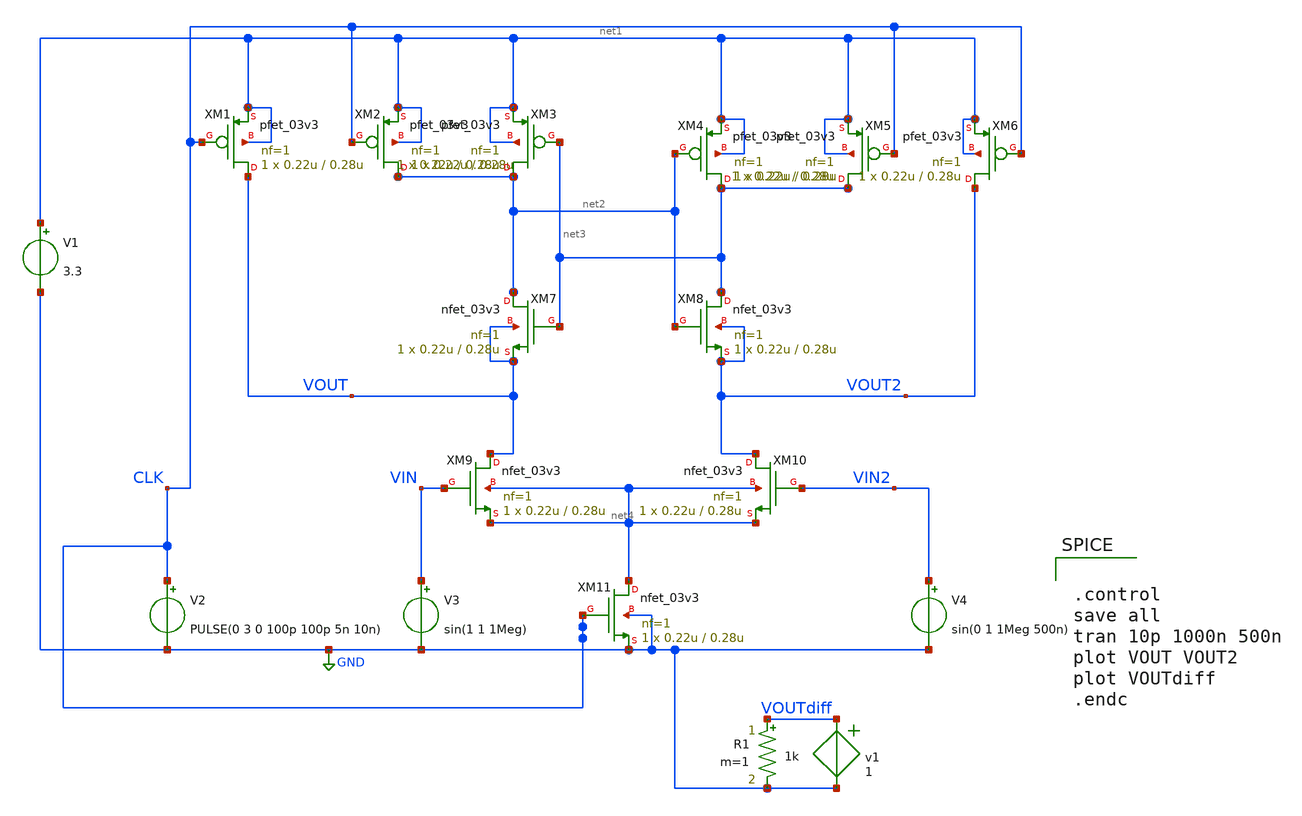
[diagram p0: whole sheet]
** sch_path: StrongARM.sch
**.subckt StrongARM
XM1 VOUT CLK net1 net1 pfet_03v3 L=0.28u W=0.22u nf=1 ad='int((nf+1)/2) * W/nf * 0.18u' as='int((nf+2)/2) * W/nf * 0.18u'
+ pd='2*int((nf+1)/2) * (W/nf + 0.18u)' ps='2*int((nf+2)/2) * (W/nf + 0.18u)' nrd='0.18u / W' nrs='0.18u / W'
+ sa=0 sb=0 sd=0 m=1
XM2 net2 CLK net1 net1 pfet_03v3 L=0.28u W=0.22u nf=1 ad='int((nf+1)/2) * W/nf * 0.18u' as='int((nf+2)/2) * W/nf * 0.18u'
+ pd='2*int((nf+1)/2) * (W/nf + 0.18u)' ps='2*int((nf+2)/2) * (W/nf + 0.18u)' nrd='0.18u / W' nrs='0.18u / W'
+ sa=0 sb=0 sd=0 m=1
XM3 net2 net3 net1 net1 pfet_03v3 L=0.28u W=0.22u nf=1 ad='int((nf+1)/2) * W/nf * 0.18u' as='int((nf+2)/2) * W/nf * 0.18u'
+ pd='2*int((nf+1)/2) * (W/nf + 0.18u)' ps='2*int((nf+2)/2) * (W/nf + 0.18u)' nrd='0.18u / W' nrs='0.18u / W'
+ sa=0 sb=0 sd=0 m=1
XM4 net3 net2 net1 net1 pfet_03v3 L=0.28u W=0.22u nf=1 ad='int((nf+1)/2) * W/nf * 0.18u' as='int((nf+2)/2) * W/nf * 0.18u'
+ pd='2*int((nf+1)/2) * (W/nf + 0.18u)' ps='2*int((nf+2)/2) * (W/nf + 0.18u)' nrd='0.18u / W' nrs='0.18u / W'
+ sa=0 sb=0 sd=0 m=1
XM5 net3 CLK net1 net1 pfet_03v3 L=0.28u W=0.22u nf=1 ad='int((nf+1)/2) * W/nf * 0.18u' as='int((nf+2)/2) * W/nf * 0.18u'
+ pd='2*int((nf+1)/2) * (W/nf + 0.18u)' ps='2*int((nf+2)/2) * (W/nf + 0.18u)' nrd='0.18u / W' nrs='0.18u / W'
+ sa=0 sb=0 sd=0 m=1
XM6 VOUT2 CLK net1 net1 pfet_03v3 L=0.28u W=0.22u nf=1 ad='int((nf+1)/2) * W/nf * 0.18u' as='int((nf+2)/2) * W/nf * 0.18u'
+ pd='2*int((nf+1)/2) * (W/nf + 0.18u)' ps='2*int((nf+2)/2) * (W/nf + 0.18u)' nrd='0.18u / W' nrs='0.18u / W'
+ sa=0 sb=0 sd=0 m=1
XM7 net2 net3 VOUT VOUT nfet_03v3 L=0.28u W=0.22u nf=1 ad='int((nf+1)/2) * W/nf * 0.18u' as='int((nf+2)/2) * W/nf * 0.18u'
+ pd='2*int((nf+1)/2) * (W/nf + 0.18u)' ps='2*int((nf+2)/2) * (W/nf + 0.18u)' nrd='0.18u / W' nrs='0.18u / W'
+ sa=0 sb=0 sd=0 m=1
XM8 net3 net2 VOUT2 VOUT2 nfet_03v3 L=0.28u W=0.22u nf=1 ad='int((nf+1)/2) * W/nf * 0.18u' as='int((nf+2)/2) * W/nf * 0.18u'
+ pd='2*int((nf+1)/2) * (W/nf + 0.18u)' ps='2*int((nf+2)/2) * (W/nf + 0.18u)' nrd='0.18u / W' nrs='0.18u / W'
+ sa=0 sb=0 sd=0 m=1
XM9 VOUT VIN net4 net4 nfet_03v3 L=0.28u W=0.22u nf=1 ad='int((nf+1)/2) * W/nf * 0.18u' as='int((nf+2)/2) * W/nf * 0.18u'
+ pd='2*int((nf+1)/2) * (W/nf + 0.18u)' ps='2*int((nf+2)/2) * (W/nf + 0.18u)' nrd='0.18u / W' nrs='0.18u / W'
+ sa=0 sb=0 sd=0 m=1
XM10 VOUT2 VIN2 net4 net4 nfet_03v3 L=0.28u W=0.22u nf=1 ad='int((nf+1)/2) * W/nf * 0.18u' as='int((nf+2)/2) * W/nf * 0.18u'
+ pd='2*int((nf+1)/2) * (W/nf + 0.18u)' ps='2*int((nf+2)/2) * (W/nf + 0.18u)' nrd='0.18u / W' nrs='0.18u / W'
+ sa=0 sb=0 sd=0 m=1
XM11 net4 CLK GND GND nfet_03v3 L=0.28u W=0.22u nf=1 ad='int((nf+1)/2) * W/nf * 0.18u' as='int((nf+2)/2) * W/nf * 0.18u'
+ pd='2*int((nf+1)/2) * (W/nf + 0.18u)' ps='2*int((nf+2)/2) * (W/nf + 0.18u)' nrd='0.18u / W' nrs='0.18u / W'
+ sa=0 sb=0 sd=0 m=1
V1 net1 GND 3.3
V2 CLK GND PULSE(0 3 0 100p 100p 5n 10n)
V3 VIN GND sin(1 1 1Meg)
V4 VIN2 GND sin(0 1 1Meg 500n)
H1 VOUTdiff GND v1 1
R1 VOUTdiff GND 1k m=1
**** begin user architecture code


.control
save all
tran 10p 1000n 500n
plot VOUT VOUT2
plot VOUTdiff
.endc


.include /foss/pdks/gf180mcuC/libs.tech/ngspice/design.ngspice
.lib /foss/pdks/gf180mcuC/libs.tech/ngspice/sm141064.ngspice typical

**** end user architecture code
**.ends
.GLOBAL GND
.end
